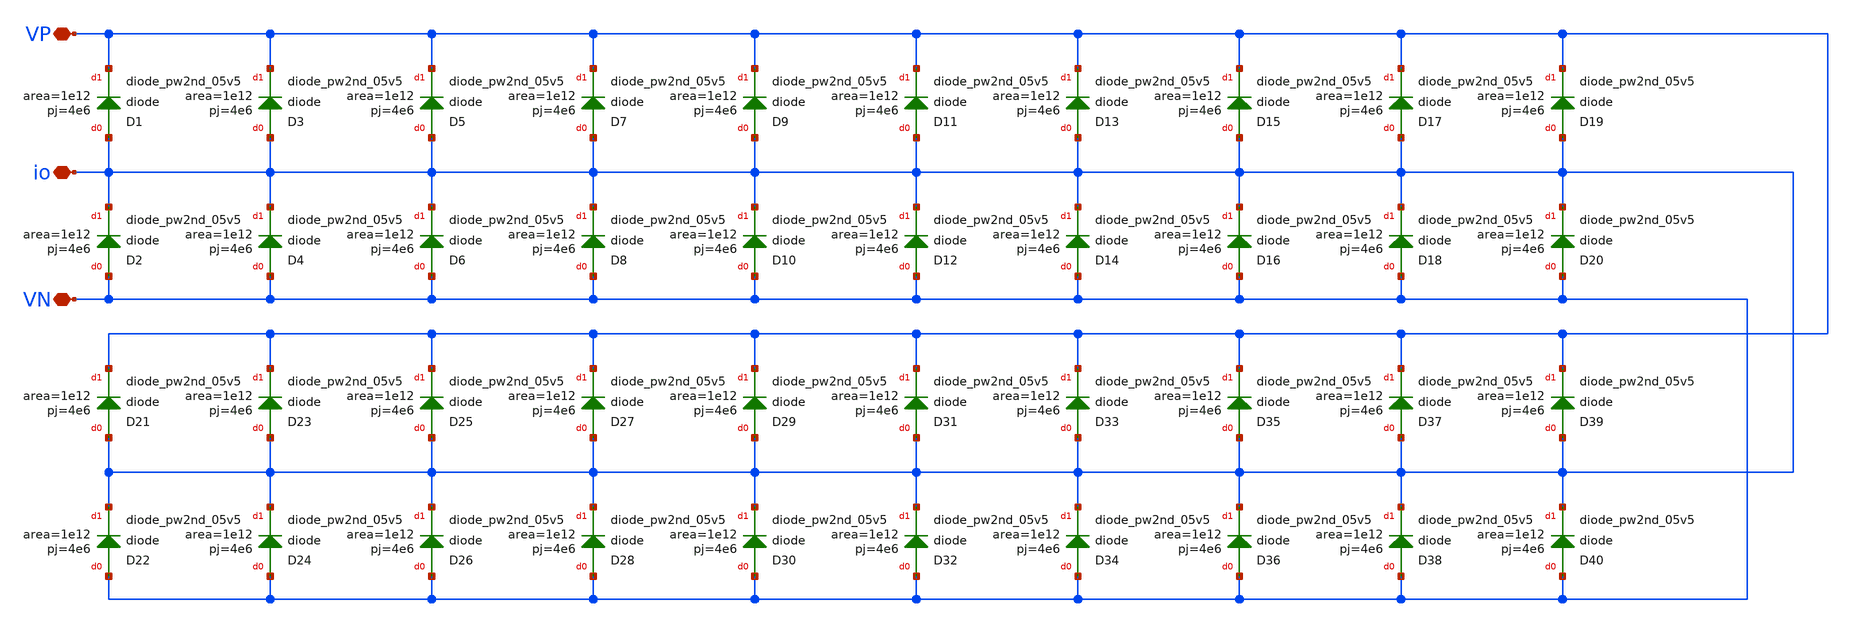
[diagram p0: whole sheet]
** sch_path: xschem/esd/esd_diodes.sch
**.subckt esd_diodes VP io VN
*.iopin VP
*.iopin io
*.iopin VN
XD1 io VP sky130_fd_pr__diode_pw2nd_05v5 area=1e12 pj=4e6
XD2 VN io sky130_fd_pr__diode_pw2nd_05v5 area=1e12 pj=4e6
XD3 io VP sky130_fd_pr__diode_pw2nd_05v5 area=1e12 pj=4e6
XD4 VN io sky130_fd_pr__diode_pw2nd_05v5 area=1e12 pj=4e6
XD5 io VP sky130_fd_pr__diode_pw2nd_05v5 area=1e12 pj=4e6
XD6 VN io sky130_fd_pr__diode_pw2nd_05v5 area=1e12 pj=4e6
XD7 io VP sky130_fd_pr__diode_pw2nd_05v5 area=1e12 pj=4e6
XD8 VN io sky130_fd_pr__diode_pw2nd_05v5 area=1e12 pj=4e6
XD9 io VP sky130_fd_pr__diode_pw2nd_05v5 area=1e12 pj=4e6
XD10 VN io sky130_fd_pr__diode_pw2nd_05v5 area=1e12 pj=4e6
XD11 io VP sky130_fd_pr__diode_pw2nd_05v5 area=1e12 pj=4e6
XD12 VN io sky130_fd_pr__diode_pw2nd_05v5 area=1e12 pj=4e6
XD13 io VP sky130_fd_pr__diode_pw2nd_05v5 area=1e12 pj=4e6
XD14 VN io sky130_fd_pr__diode_pw2nd_05v5 area=1e12 pj=4e6
XD15 io VP sky130_fd_pr__diode_pw2nd_05v5 area=1e12 pj=4e6
XD16 VN io sky130_fd_pr__diode_pw2nd_05v5 area=1e12 pj=4e6
XD17 io VP sky130_fd_pr__diode_pw2nd_05v5 area=1e12 pj=4e6
XD18 VN io sky130_fd_pr__diode_pw2nd_05v5 area=1e12 pj=4e6
XD19 io VP sky130_fd_pr__diode_pw2nd_05v5 area=1e12 pj=4e6
XD20 VN io sky130_fd_pr__diode_pw2nd_05v5 area=1e12 pj=4e6
XD21 io VP sky130_fd_pr__diode_pw2nd_05v5 area=1e12 pj=4e6
XD22 VN io sky130_fd_pr__diode_pw2nd_05v5 area=1e12 pj=4e6
XD23 io VP sky130_fd_pr__diode_pw2nd_05v5 area=1e12 pj=4e6
XD24 VN io sky130_fd_pr__diode_pw2nd_05v5 area=1e12 pj=4e6
XD25 io VP sky130_fd_pr__diode_pw2nd_05v5 area=1e12 pj=4e6
XD26 VN io sky130_fd_pr__diode_pw2nd_05v5 area=1e12 pj=4e6
XD27 io VP sky130_fd_pr__diode_pw2nd_05v5 area=1e12 pj=4e6
XD28 VN io sky130_fd_pr__diode_pw2nd_05v5 area=1e12 pj=4e6
XD29 io VP sky130_fd_pr__diode_pw2nd_05v5 area=1e12 pj=4e6
XD30 VN io sky130_fd_pr__diode_pw2nd_05v5 area=1e12 pj=4e6
XD31 io VP sky130_fd_pr__diode_pw2nd_05v5 area=1e12 pj=4e6
XD32 VN io sky130_fd_pr__diode_pw2nd_05v5 area=1e12 pj=4e6
XD33 io VP sky130_fd_pr__diode_pw2nd_05v5 area=1e12 pj=4e6
XD34 VN io sky130_fd_pr__diode_pw2nd_05v5 area=1e12 pj=4e6
XD35 io VP sky130_fd_pr__diode_pw2nd_05v5 area=1e12 pj=4e6
XD36 VN io sky130_fd_pr__diode_pw2nd_05v5 area=1e12 pj=4e6
XD37 io VP sky130_fd_pr__diode_pw2nd_05v5 area=1e12 pj=4e6
XD38 VN io sky130_fd_pr__diode_pw2nd_05v5 area=1e12 pj=4e6
XD39 io VP sky130_fd_pr__diode_pw2nd_05v5 area=1e12 pj=4e6
XD40 VN io sky130_fd_pr__diode_pw2nd_05v5 area=1e12 pj=4e6
**.ends
.end
